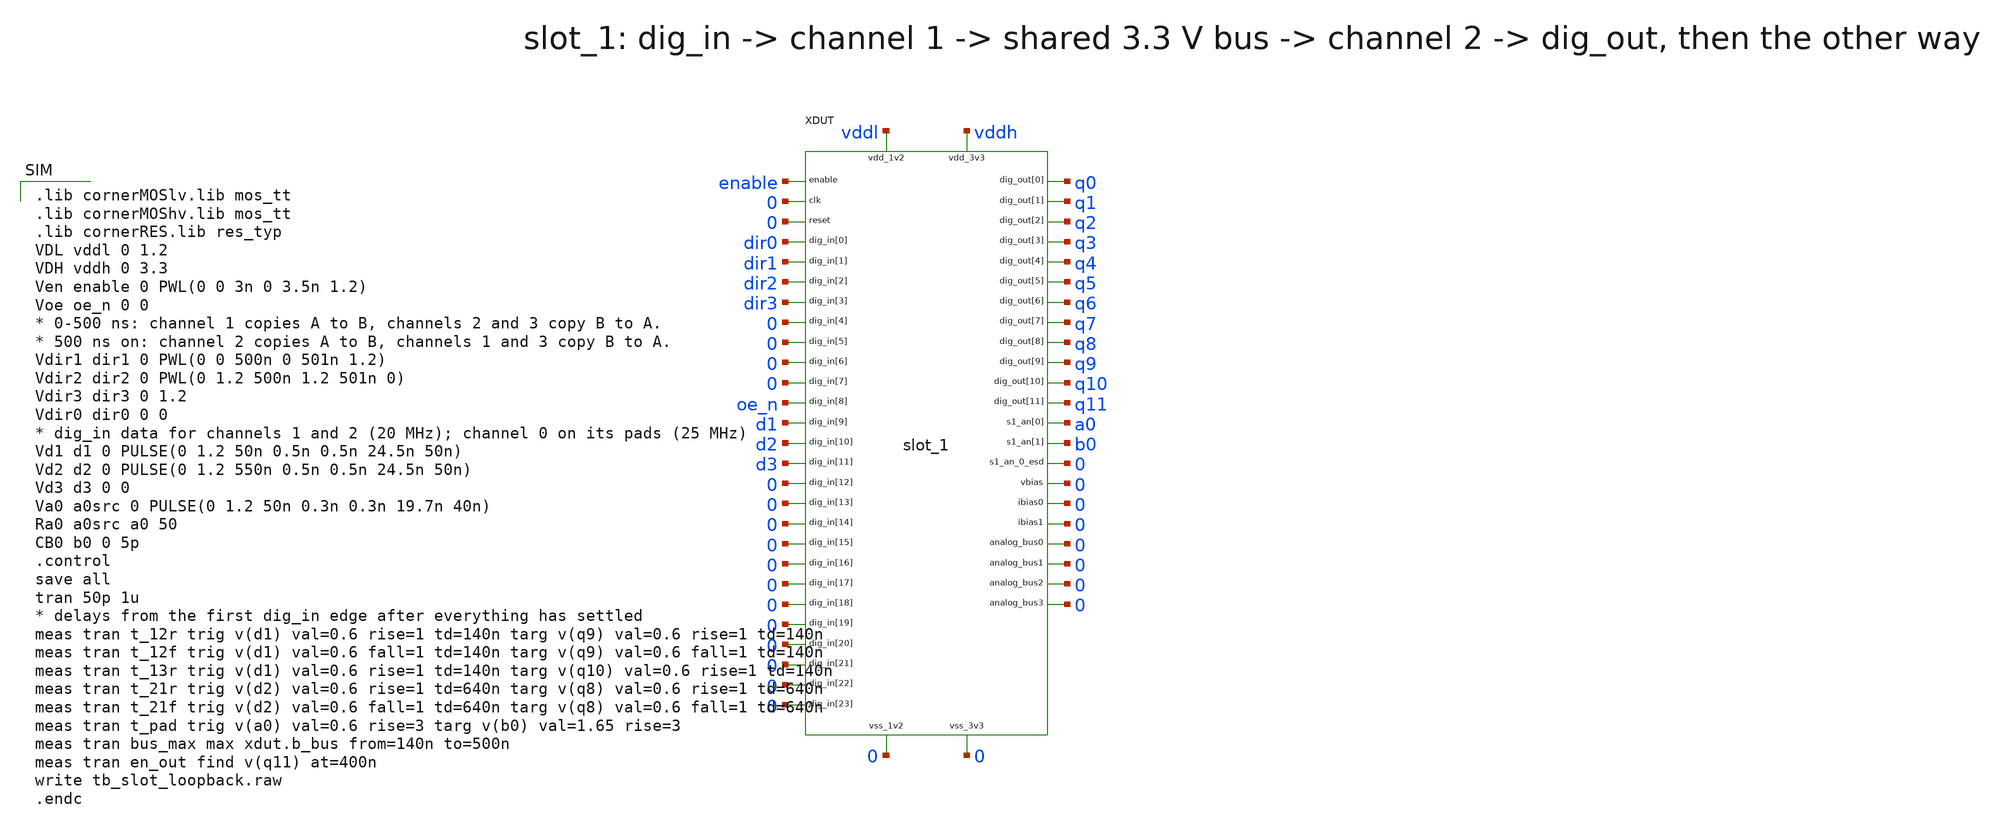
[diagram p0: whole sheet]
** sch_path: verification/tb_slot_loopback.sch
**.subckt tb_slot_loopback
XDUT vddl vddh 0 0 enable 0 0 dir0 dir1 dir2 dir3 0 0 0 0 oe_n d1 d2 d3 0 0 0 0 0 0 0 0 0 0 0 0 q0
+ q1 q2 q3 q4 q5 q6 q7 q8 q9 q10 q11 a0 b0 0 0 0 0 0 0 0 0 slot_1
**** begin user architecture code

.lib cornerMOSlv.lib mos_tt
.lib cornerMOShv.lib mos_tt
.lib cornerRES.lib res_typ
VDL vddl 0 1.2
VDH vddh 0 3.3
Ven enable 0 PWL(0 0 3n 0 3.5n 1.2)
Voe oe_n 0 0
* 0-500 ns: channel 1 copies A to B, channels 2 and 3 copy B to A.
* 500 ns on: channel 2 copies A to B, channels 1 and 3 copy B to A.
Vdir1 dir1 0 PWL(0 0 500n 0 501n 1.2)
Vdir2 dir2 0 PWL(0 1.2 500n 1.2 501n 0)
Vdir3 dir3 0 1.2
Vdir0 dir0 0 0
* dig_in data for channels 1 and 2 (20 MHz); channel 0 on its pads (25 MHz)
Vd1 d1 0 PULSE(0 1.2 50n 0.5n 0.5n 24.5n 50n)
Vd2 d2 0 PULSE(0 1.2 550n 0.5n 0.5n 24.5n 50n)
Vd3 d3 0 0
Va0 a0src 0 PULSE(0 1.2 50n 0.3n 0.3n 19.7n 40n)
Ra0 a0src a0 50
CB0 b0 0 5p
.control
save all
tran 50p 1u
* delays from the first dig_in edge after everything has settled
meas tran t_12r trig v(d1) val=0.6 rise=1 td=140n targ v(q9) val=0.6 rise=1 td=140n
meas tran t_12f trig v(d1) val=0.6 fall=1 td=140n targ v(q9) val=0.6 fall=1 td=140n
meas tran t_13r trig v(d1) val=0.6 rise=1 td=140n targ v(q10) val=0.6 rise=1 td=140n
meas tran t_21r trig v(d2) val=0.6 rise=1 td=640n targ v(q8) val=0.6 rise=1 td=640n
meas tran t_21f trig v(d2) val=0.6 fall=1 td=640n targ v(q8) val=0.6 fall=1 td=640n
meas tran t_pad trig v(a0) val=0.6 rise=3 targ v(b0) val=1.65 rise=3
meas tran bus_max max xdut.b_bus from=140n to=500n
meas tran en_out find v(q11) at=400n
write tb_slot_loopback.raw
.endc

**** end user architecture code
**.ends
.end
